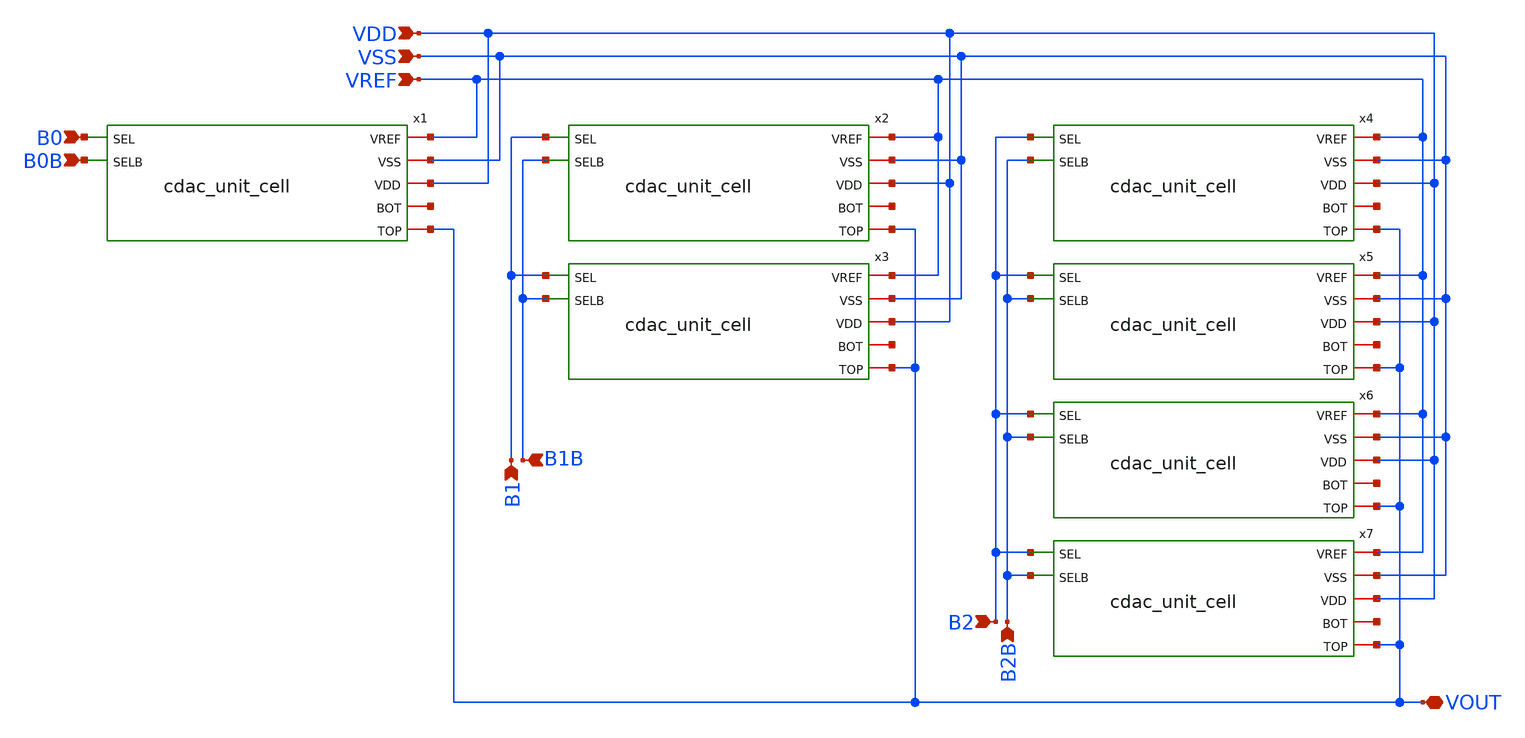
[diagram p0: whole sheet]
** sch_path: designs/libs/core_matchmaker/7d_cdac_3b_single/7d_cdac_3b_single.sch
**.subckt 7d_cdac_3b_single VOUT VREF VSS VDD B0B B0 B1 B1B B2B B2
*.iopin VOUT
*.ipin VREF
*.ipin VSS
*.ipin VDD
*.ipin B0B
*.ipin B0
*.ipin B1
*.ipin B1B
*.ipin B2B
*.ipin B2
x1 B0 VREF VSS B0B VDD net1 VOUT cdac_unit_cell
x2 B1 VREF VSS B1B VDD net2 VOUT cdac_unit_cell
x3 B1 VREF VSS B1B VDD net3 VOUT cdac_unit_cell
x4 B2 VREF VSS B2B VDD net4 VOUT cdac_unit_cell
x5 B2 VREF VSS B2B VDD net5 VOUT cdac_unit_cell
x6 B2 VREF VSS B2B VDD net6 VOUT cdac_unit_cell
x7 B2 VREF VSS B2B VDD net7 VOUT cdac_unit_cell
**.ends
.end
